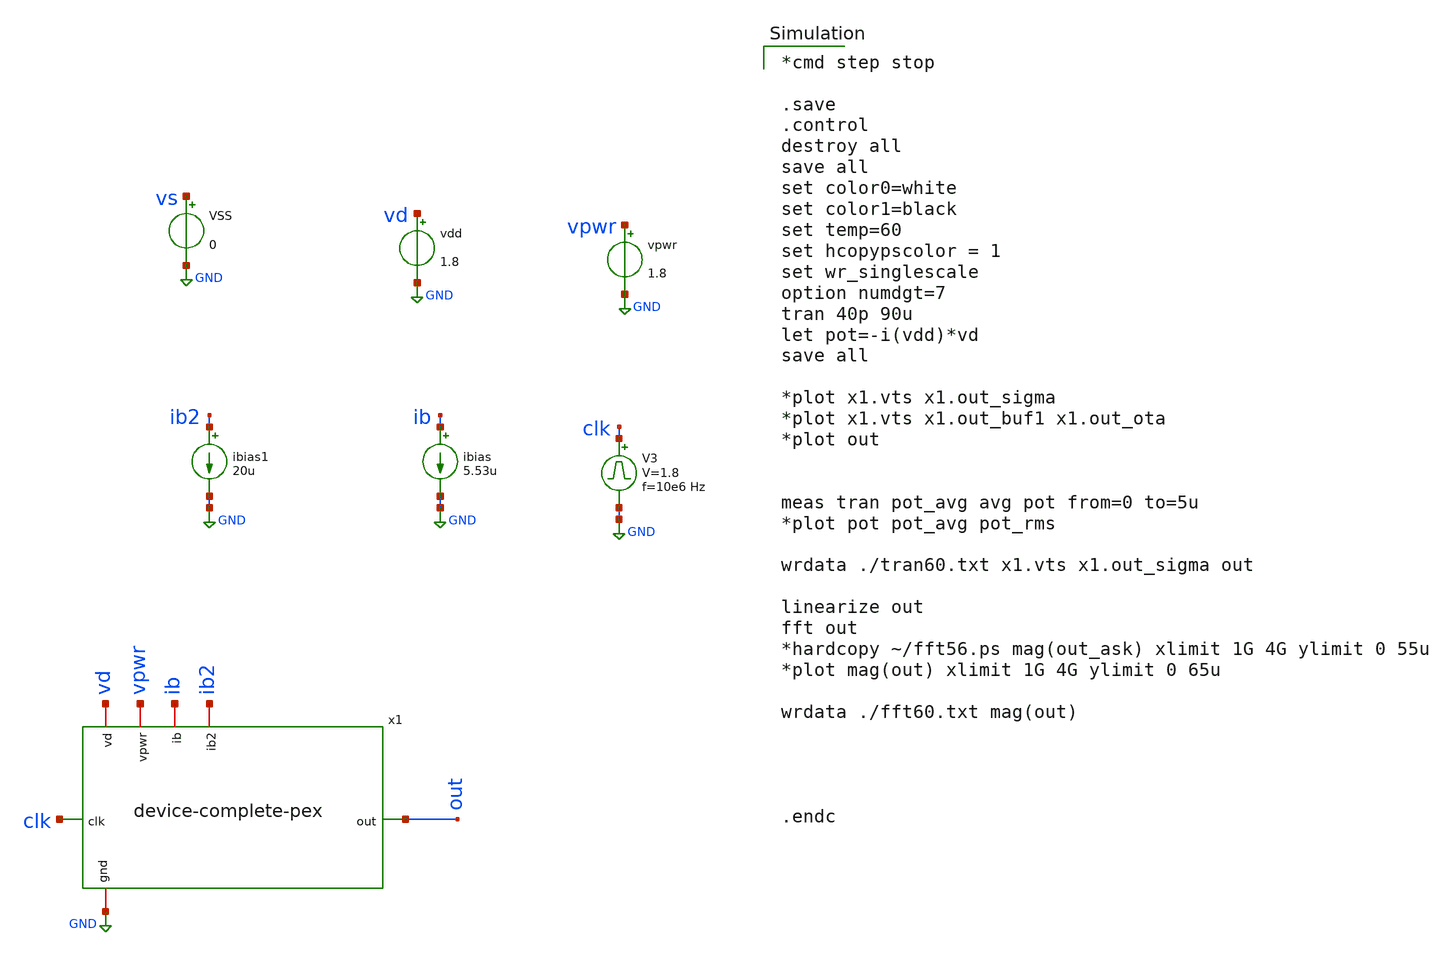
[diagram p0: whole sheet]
** sch_path: device-complete/xschem/device-complete-tb3.sch
**.subckt device-complete-tb3
vpwr vpwr GND 1.8
V3 clk GND pulse 0 1.8 '0.495/ 10e6 ' '0.01/10e6 ' '0.01/10e6 ' '0.49/10e6 ' '1/10e6 '
vdd vd GND 1.8
ibias ib GND 5.53u
VSS vs GND 0
ibias1 ib2 GND 20u
x1 vd clk out vpwr ib ib2 GND device-complete-pex
**** begin user architecture code

*cmd step stop

.save
.control
destroy all
save all
set color0=white
set color1=black
set temp=60
set hcopypscolor = 1
set wr_singlescale
option numdgt=7
tran 40p 90u
let pot=-i(vdd)*vd
save all

*plot x1.vts x1.out_sigma
*plot x1.vts x1.out_buf1 x1.out_ota
*plot out


meas tran pot_avg avg pot from=0 to=5u
*plot pot pot_avg pot_rms

wrdata ./tran60.txt x1.vts x1.out_sigma out

linearize out
fft out
*hardcopy ~/fft56.ps mag(out_ask) xlimit 1G 4G ylimit 0 55u
*plot mag(out) xlimit 1G 4G ylimit 0 65u

wrdata ./fft60.txt mag(out)




.endc



 .lib $::SKYWATER_MODELS/sky130.lib.spice tt
.include $::SKYWATER_STDCELLS/sky130_fd_sc_hd.spice

**** end user architecture code
**.ends
.GLOBAL GND
.end
